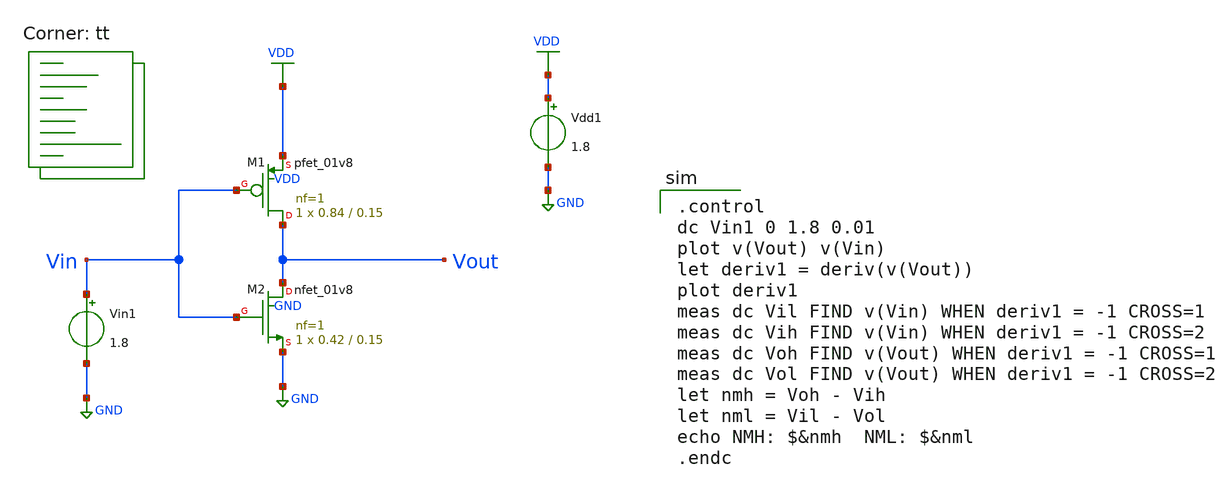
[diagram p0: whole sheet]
** sch_path: tutorial-2/source/q1a.sch
**.subckt q1a
XM1 Vout Vin VDD VDD sky130_fd_pr__pfet_01v8 L=0.15 W=0.84 nf=1 ad='int((nf+1)/2) * W/nf * 0.29' as='int((nf+2)/2) * W/nf * 0.29'
+ pd='2*int((nf+1)/2) * (W/nf + 0.29)' ps='2*int((nf+2)/2) * (W/nf + 0.29)' nrd='0.29 / W' nrs='0.29 / W'
+ sa=0 sb=0 sd=0 mult=1 m=1
XM2 Vout Vin GND GND sky130_fd_pr__nfet_01v8 L=0.15 W=0.42 nf=1 ad='int((nf+1)/2) * W/nf * 0.29' as='int((nf+2)/2) * W/nf * 0.29'
+ pd='2*int((nf+1)/2) * (W/nf + 0.29)' ps='2*int((nf+2)/2) * (W/nf + 0.29)' nrd='0.29 / W' nrs='0.29 / W'
+ sa=0 sb=0 sd=0 mult=1 m=1
Vdd1 VDD GND 1.8
Vin1 Vin GND 1.8
**** begin user architecture code
.lib $::SKYWATER_MODELS/sky130.lib.spice tt

.control
dc Vin1 0 1.8 0.01
plot v(Vout) v(Vin)
let deriv1 = deriv(v(Vout))
plot deriv1
meas dc Vil FIND v(Vin) WHEN deriv1 = -1 CROSS=1
meas dc Vih FIND v(Vin) WHEN deriv1 = -1 CROSS=2
meas dc Voh FIND v(Vout) WHEN deriv1 = -1 CROSS=1
meas dc Vol FIND v(Vout) WHEN deriv1 = -1 CROSS=2
let nmh = Voh - Vih
let nml = Vil - Vol
echo NMH: $&nmh  NML: $&nml
.endc

**** end user architecture code
**.ends
.GLOBAL VDD
.GLOBAL GND
.end
